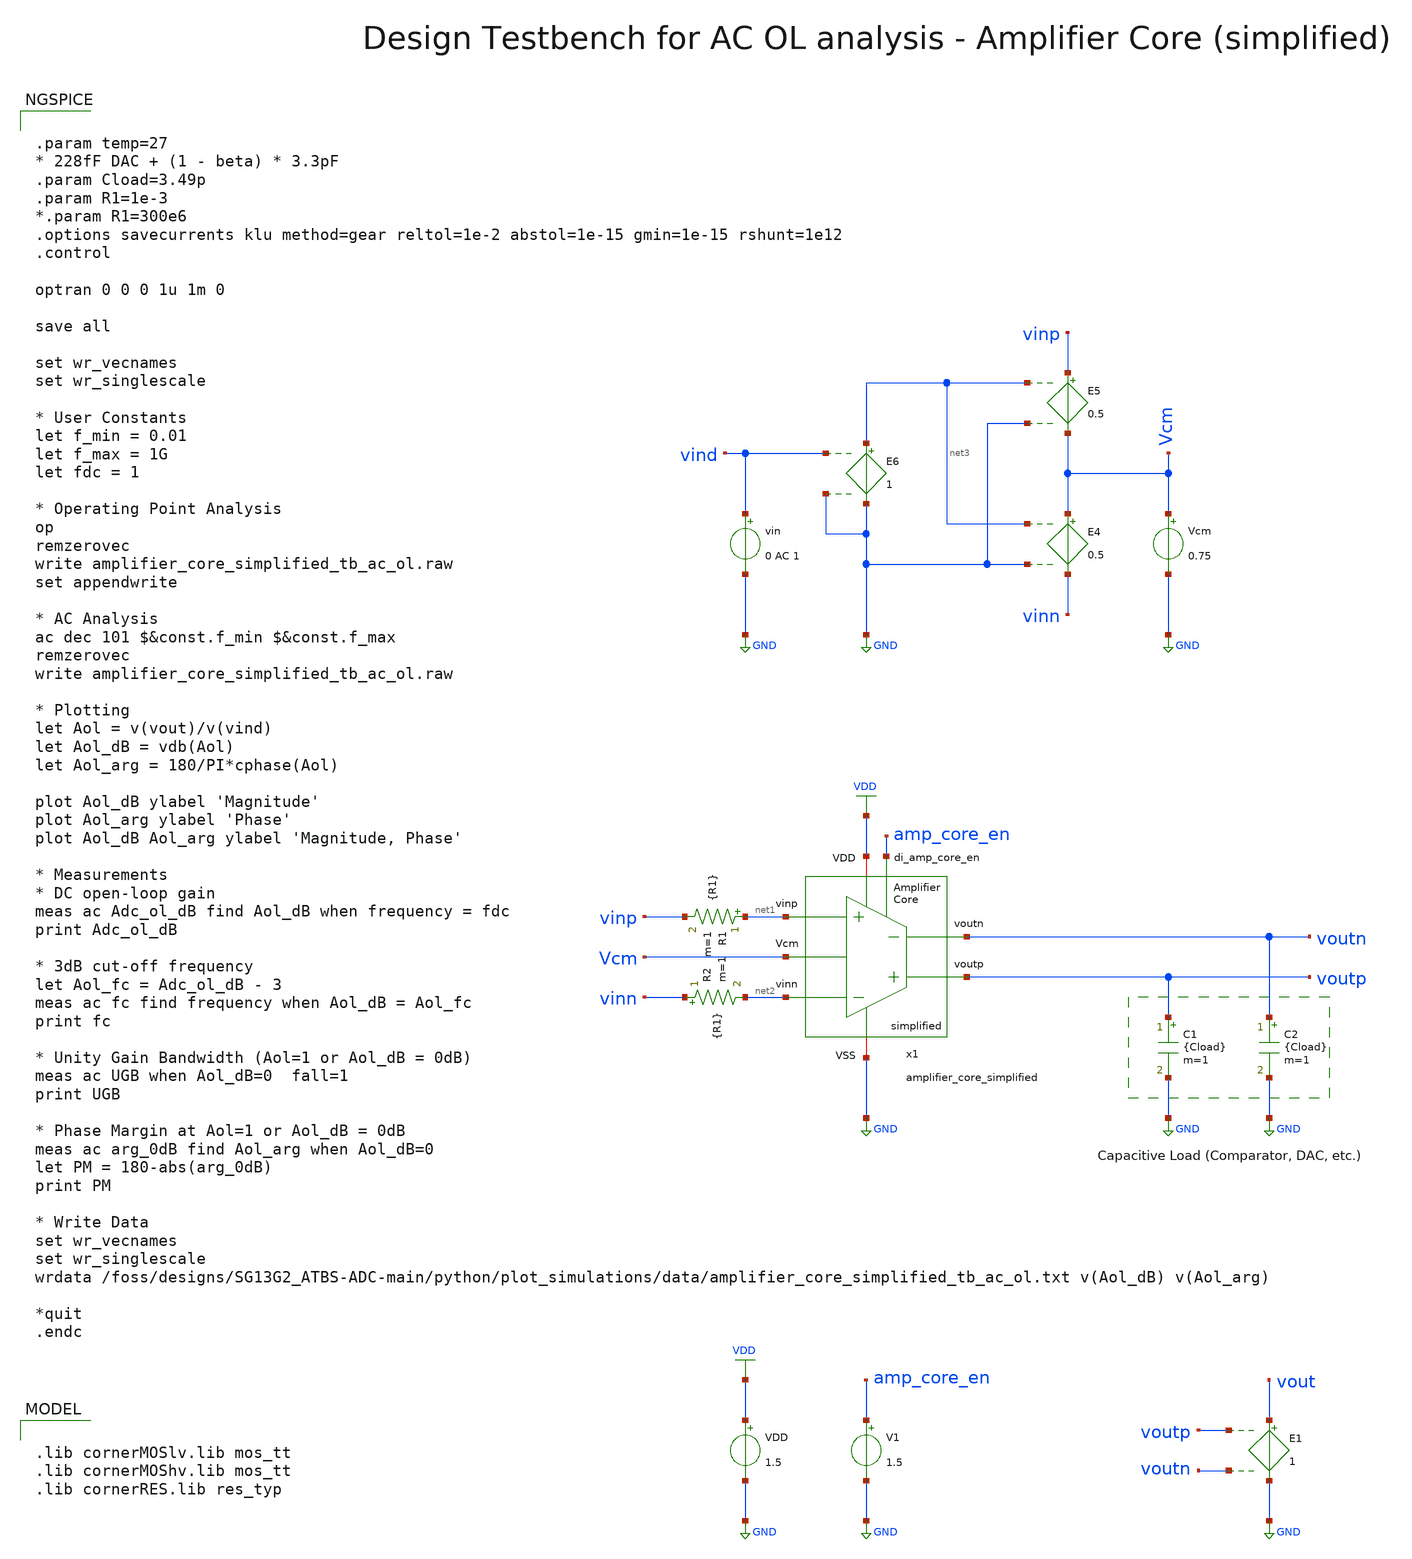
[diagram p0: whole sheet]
** sch_path: SG13G2_ATBS-ADC-main/xschem/bio_amplifier/amplifier_core/testbenches/amplifier_core_simplified_tb_ac_ol.sch
**.subckt amplifier_core_simplified_tb_ac_ol
VDD VDD GND 1.5
C1 voutp GND {Cload} m=1
C2 voutn GND {Cload} m=1
Vcm Vcm GND 0.75
E4 Vcm vinn net3 GND 0.5
E5 vinp Vcm net3 GND 0.5
E6 net3 GND vind GND 1
V1 amp_core_en GND 1.5
E1 vout GND voutp voutn 1
vin vind GND 0 AC 1
x1 voutp voutn amp_core_en net2 net1 VDD GND Vcm amplifier_core_simplified
R1 net1 vinp {R1} m=1
R2 vinn net2 {R1} m=1
**** begin user architecture code


.param temp=27
* 228fF DAC + (1 - beta) * 3.3pF
.param Cload=3.49p
.param R1=1e-3
*.param R1=300e6
.options savecurrents klu method=gear reltol=1e-2 abstol=1e-15 gmin=1e-15 rshunt=1e12
.control

optran 0 0 0 1u 1m 0

save all

set wr_vecnames
set wr_singlescale

* User Constants
let f_min = 0.01
let f_max = 1G
let fdc = 1

* Operating Point Analysis
op
remzerovec
write amplifier_core_simplified_tb_ac_ol.raw
set appendwrite

* AC Analysis
ac dec 101 $&const.f_min $&const.f_max
remzerovec
write amplifier_core_simplified_tb_ac_ol.raw

* Plotting
let Aol = v(vout)/v(vind)
let Aol_dB = vdb(Aol)
let Aol_arg = 180/PI*cphase(Aol)

plot Aol_dB ylabel 'Magnitude'
plot Aol_arg ylabel 'Phase'
plot Aol_dB Aol_arg ylabel 'Magnitude, Phase'

* Measurements
* DC open-loop gain
meas ac Adc_ol_dB find Aol_dB when frequency = fdc
print Adc_ol_dB

* 3dB cut-off frequency
let Aol_fc = Adc_ol_dB - 3
meas ac fc find frequency when Aol_dB = Aol_fc
print fc

* Unity Gain Bandwidth (Aol=1 or Aol_dB = 0dB)
meas ac UGB when Aol_dB=0  fall=1
print UGB

* Phase Margin at Aol=1 or Aol_dB = 0dB
meas ac arg_0dB find Aol_arg when Aol_dB=0
let PM = 180-abs(arg_0dB)
print PM

* Write Data
set wr_vecnames
set wr_singlescale
wrdata
+ /foss/designs/SG13G2_ATBS-ADC-main/python/plot_simulations/data/amplifier_core_simplified_tb_ac_ol.txt v(Aol_dB) v(Aol_arg)

*quit
.endc



.lib cornerMOSlv.lib mos_tt
.lib cornerMOShv.lib mos_tt
.lib cornerRES.lib res_typ

**** end user architecture code
**.ends
.GLOBAL GND
.GLOBAL VDD
.end
